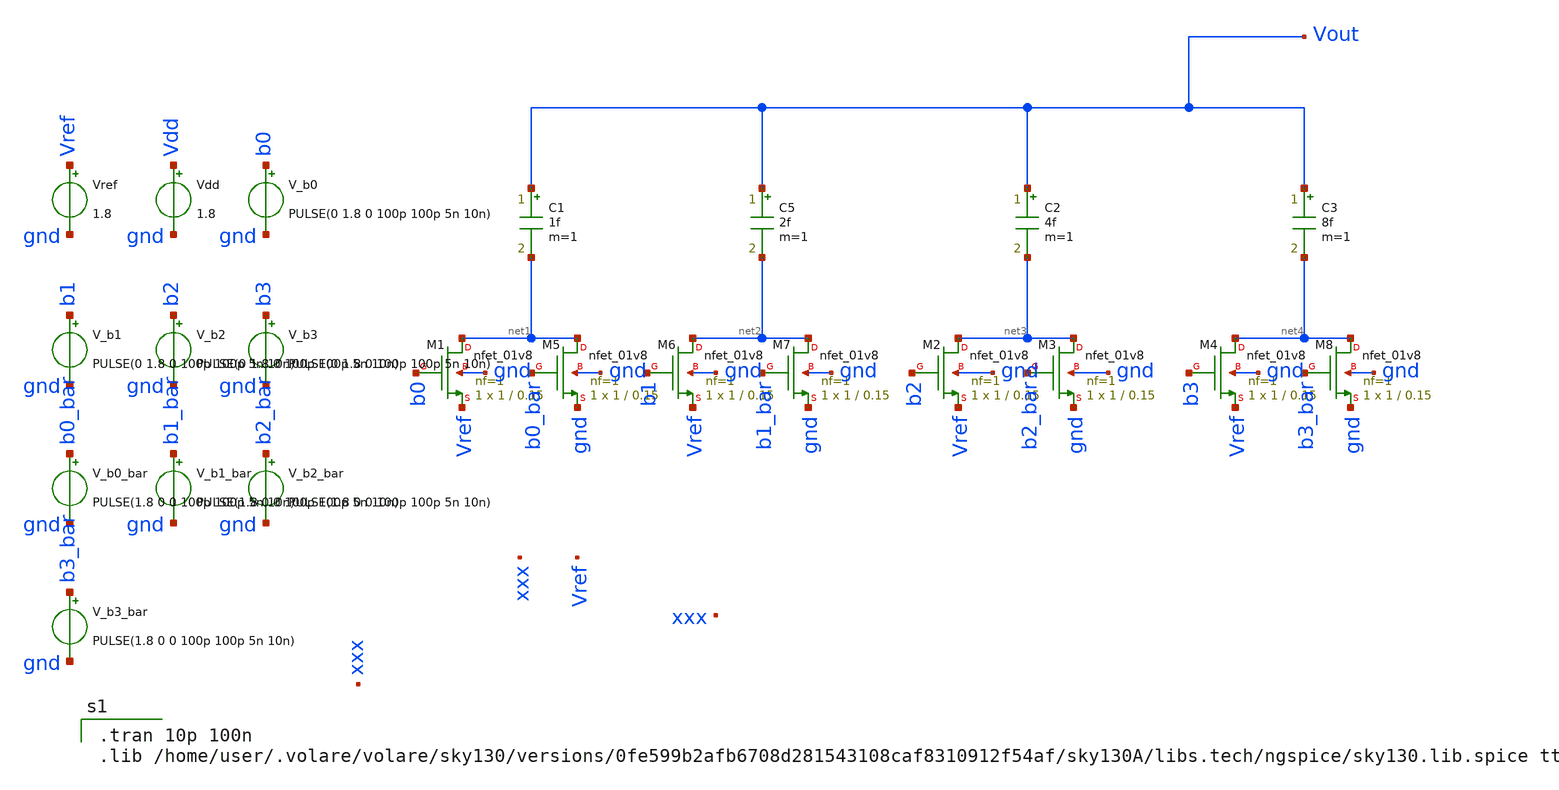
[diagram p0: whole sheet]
** sch_path: sar_adc_dac_switching/conv.sch
**.subckt conv
C1 Vout net1 1f m=1
XM1 net1 b0 Vref gnd sky130_fd_pr__nfet_01v8 L=0.15 W=1 nf=1 ad='int((nf+1)/2) * W/nf * 0.29' as='int((nf+2)/2) * W/nf * 0.29'
+ pd='2*int((nf+1)/2) * (W/nf + 0.29)' ps='2*int((nf+2)/2) * (W/nf + 0.29)' nrd='0.29 / W' nrs='0.29 / W'
+ sa=0 sb=0 sd=0 mult=1 m=1
XM5 net1 b0_bar gnd gnd sky130_fd_pr__nfet_01v8 L=0.15 W=1 nf=1 ad='int((nf+1)/2) * W/nf * 0.29' as='int((nf+2)/2) * W/nf * 0.29'
+ pd='2*int((nf+1)/2) * (W/nf + 0.29)' ps='2*int((nf+2)/2) * (W/nf + 0.29)' nrd='0.29 / W' nrs='0.29 / W'
+ sa=0 sb=0 sd=0 mult=1 m=1
C5 Vout net2 2f m=1
XM6 net2 b1 Vref gnd sky130_fd_pr__nfet_01v8 L=0.15 W=1 nf=1 ad='int((nf+1)/2) * W/nf * 0.29' as='int((nf+2)/2) * W/nf * 0.29'
+ pd='2*int((nf+1)/2) * (W/nf + 0.29)' ps='2*int((nf+2)/2) * (W/nf + 0.29)' nrd='0.29 / W' nrs='0.29 / W'
+ sa=0 sb=0 sd=0 mult=1 m=1
XM7 net2 b1_bar gnd gnd sky130_fd_pr__nfet_01v8 L=0.15 W=1 nf=1 ad='int((nf+1)/2) * W/nf * 0.29' as='int((nf+2)/2) * W/nf * 0.29'
+ pd='2*int((nf+1)/2) * (W/nf + 0.29)' ps='2*int((nf+2)/2) * (W/nf + 0.29)' nrd='0.29 / W' nrs='0.29 / W'
+ sa=0 sb=0 sd=0 mult=1 m=1
C2 Vout net3 4f m=1
XM2 net3 b2 Vref gnd sky130_fd_pr__nfet_01v8 L=0.15 W=1 nf=1 ad='int((nf+1)/2) * W/nf * 0.29' as='int((nf+2)/2) * W/nf * 0.29'
+ pd='2*int((nf+1)/2) * (W/nf + 0.29)' ps='2*int((nf+2)/2) * (W/nf + 0.29)' nrd='0.29 / W' nrs='0.29 / W'
+ sa=0 sb=0 sd=0 mult=1 m=1
XM3 net3 b2_bar gnd gnd sky130_fd_pr__nfet_01v8 L=0.15 W=1 nf=1 ad='int((nf+1)/2) * W/nf * 0.29' as='int((nf+2)/2) * W/nf * 0.29'
+ pd='2*int((nf+1)/2) * (W/nf + 0.29)' ps='2*int((nf+2)/2) * (W/nf + 0.29)' nrd='0.29 / W' nrs='0.29 / W'
+ sa=0 sb=0 sd=0 mult=1 m=1
C3 Vout net4 8f m=1
XM4 net4 b3 Vref gnd sky130_fd_pr__nfet_01v8 L=0.15 W=1 nf=1 ad='int((nf+1)/2) * W/nf * 0.29' as='int((nf+2)/2) * W/nf * 0.29'
+ pd='2*int((nf+1)/2) * (W/nf + 0.29)' ps='2*int((nf+2)/2) * (W/nf + 0.29)' nrd='0.29 / W' nrs='0.29 / W'
+ sa=0 sb=0 sd=0 mult=1 m=1
XM8 net4 b3_bar gnd gnd sky130_fd_pr__nfet_01v8 L=0.15 W=1 nf=1 ad='int((nf+1)/2) * W/nf * 0.29' as='int((nf+2)/2) * W/nf * 0.29'
+ pd='2*int((nf+1)/2) * (W/nf + 0.29)' ps='2*int((nf+2)/2) * (W/nf + 0.29)' nrd='0.29 / W' nrs='0.29 / W'
+ sa=0 sb=0 sd=0 mult=1 m=1
Vref Vref gnd 1.8
Vdd Vdd gnd 1.8
V_b0 b0 gnd PULSE(0 1.8 0 100p 100p 5n 10n)
V_b1 b1 gnd PULSE(0 1.8 0 100p 100p 5n 10n)
V_b2 b2 gnd PULSE(0 1.8 0 100p 100p 5n 10n)
V_b3 b3 gnd PULSE(0 1.8 0 100p 100p 5n 10n)
V_b0_bar b0_bar gnd PULSE(1.8 0 0 100p 100p 5n 10n)
V_b1_bar b1_bar gnd PULSE(1.8 0 0 100p 100p 5n 10n)
V_b2_bar b2_bar gnd PULSE(1.8 0 0 100p 100p 5n 10n)
V_b3_bar b3_bar gnd PULSE(1.8 0 0 100p 100p 5n 10n)
**** begin user architecture code

.tran 10p 100n
.lib /home/user/.volare/volare/sky130/versions/0fe599b2afb6708d281543108caf8310912f54af/sky130A/libs.tech/ngspice/sky130.lib.spice tt

**** end user architecture code
**.ends
.end
